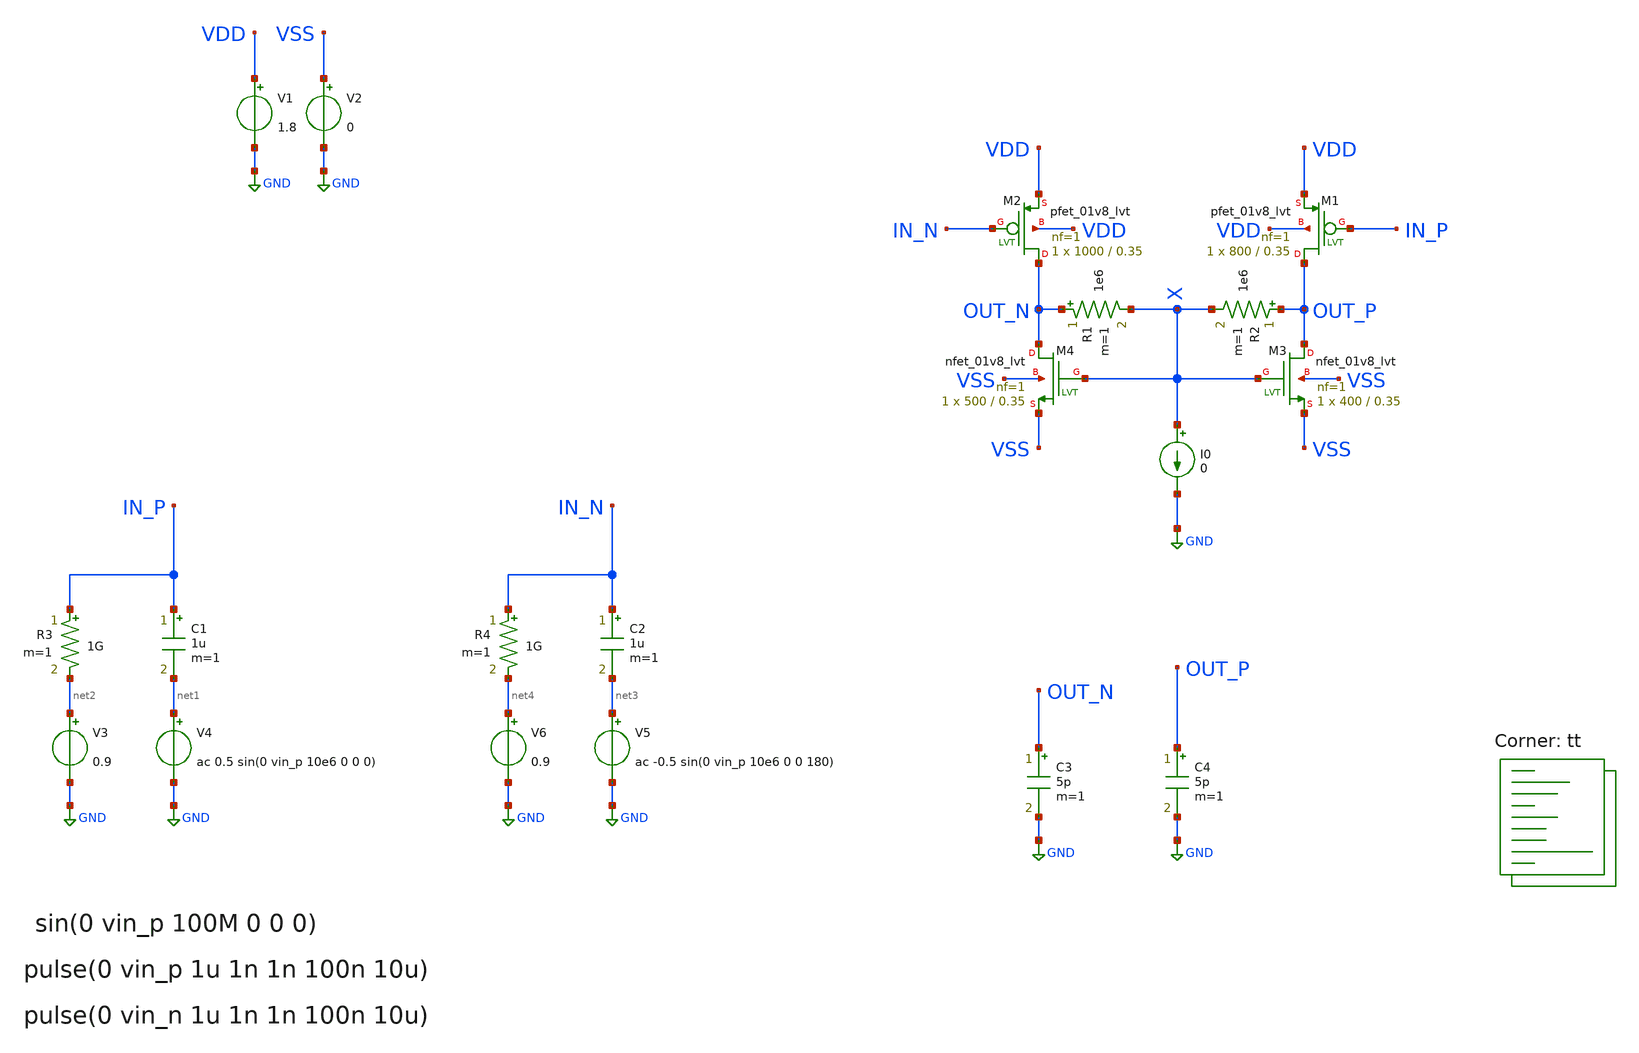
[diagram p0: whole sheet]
** sch_path: xschem/common_source.sch
**.subckt common_source
V1 VDD GND 1.8
.save i(v1)
V2 VSS GND 0
.save i(v2)
V4 net1 GND ac 0.5 sin(0 vin_p 10e6 0 0 0)
.save i(v4)
XM1 OUT_P IN_P VDD VDD sky130_fd_pr__pfet_01v8_lvt L=0.35 W=800 nf=1 ad='int((1 + 1)/2) * 800 / 1 * 0.29'
+ as='int((1 + 2)/2) * 800 / 1 * 0.29' pd='2*int((1 + 1)/2) * (800 / 1 + 0.29)' ps='2*int((1 + 2)/2) * (800 / 1 + 0.29)'
+ nrd='0.29 / 800 ' nrs='0.29 / 800 ' sa=0 sb=0 sd=0 mult=1 m=1
XM2 OUT_N IN_N VDD VDD sky130_fd_pr__pfet_01v8_lvt L=0.35 W=1000 nf=1 ad='int((1 + 1)/2) * 1000 / 1 * 0.29'
+ as='int((1 + 2)/2) * 1000 / 1 * 0.29' pd='2*int((1 + 1)/2) * (1000 / 1 + 0.29)' ps='2*int((1 + 2)/2) * (1000 / 1 + 0.29)'
+ nrd='0.29 / 1000 ' nrs='0.29 / 1000 ' sa=0 sb=0 sd=0 mult=1 m=1
XM3 OUT_P X VSS VSS sky130_fd_pr__nfet_01v8_lvt L=0.35 W=400 nf=1 ad='int((1 + 1)/2) * 400 / 1 * 0.29'
+ as='int((1 + 2)/2) * 400 / 1 * 0.29' pd='2*int((1 + 1)/2) * (400 / 1 + 0.29)' ps='2*int((1 + 2)/2) * (400 / 1 + 0.29)'
+ nrd='0.29 / 400 ' nrs='0.29 / 400 ' sa=0 sb=0 sd=0 mult=1 m=1
XM4 OUT_N X VSS VSS sky130_fd_pr__nfet_01v8_lvt L=0.35 W=500 nf=1 ad='int((1 + 1)/2) * 500 / 1 * 0.29'
+ as='int((1 + 2)/2) * 500 / 1 * 0.29' pd='2*int((1 + 1)/2) * (500 / 1 + 0.29)' ps='2*int((1 + 2)/2) * (500 / 1 + 0.29)'
+ nrd='0.29 / 500 ' nrs='0.29 / 500 ' sa=0 sb=0 sd=0 mult=1 m=1
I0 X GND 0
R1 OUT_N X 1e6 m=1
R2 OUT_P X 1e6 m=1
C1 IN_P net1 1u m=1
V3 net2 GND 0.9
.save i(v3)
R3 IN_P net2 1G m=1
V5 net3 GND ac -0.5 sin(0 vin_p 10e6 0 0 180)
.save i(v5)
C2 IN_N net3 1u m=1
V6 net4 GND 0.9
.save i(v6)
R4 IN_N net4 1G m=1
C3 OUT_N GND 5p m=1
C4 OUT_P GND 5p m=1
**** begin user architecture code


.temp 25

.param vin_p=1
.param vin_n= -1 * vin_p

.control
option savecurrents
option klu
option method=gear
option noacct
option noinit
save all


save @m.xm1.msky130_fd_pr__pfet_01v8_lvt[gm]
save @m.xm1.msky130_fd_pr__pfet_01v8_lvt[id]
save @m.xm1.msky130_fd_pr__pfet_01v8_lvt[vds]

save @m.xm2.msky130_fd_pr__pfet_01v8_lvt[gm]
save @m.xm2.msky130_fd_pr__pfet_01v8_lvt[id]
save @m.xm2.msky130_fd_pr__pfet_01v8_lvt[vds]

save @m.xm3.msky130_fd_pr__nfet_01v8_lvt[gm]
save @m.xm3.msky130_fd_pr__nfet_01v8_lvt[id]
save @m.xm3.msky130_fd_pr__nfet_01v8_lvt[vds]

save @m.xm4.msky130_fd_pr__nfet_01v8_lvt[gm]
save @m.xm4.msky130_fd_pr__nfet_01v8_lvt[id]
save @m.xm4.msky130_fd_pr__nfet_01v8_lvt[vds]




op
write common_source.raw

*vb1 sweep
*dc v3 0 1.8 0.1
*plot out_p
*plot @m.xm3.msky130_fd_pr__nfet_01v8_lvt[vds]

*vb2 sweep
*dc v4 0 1.8 0.1
*plot out_p
*plot @m.xm5.msky130_fd_pr__pfet_01v8_lvt[vds]

*vb3 sweep
*dc v5 0 1.8 0.1
*plot out_p
*plot @m.xm7.msky130_fd_pr__pfet_01v8_lvt[vds]

ac dec 10 1k 10G
let out_db = db(mag(out_p - out_n))
let out_ph = phase(out_p - out_n) / pi * 180
plot out_db
*plot out_ph
meas ac w_u WHEN out_db=0
meas ac p_x WHEN out_ph=0
meas ac phase_mar find out_ph AT=w_u
let w_u_mhz = w_u / 1e6
print w_u_mhz phase_mar

*dc i0 0 1u 1n
*plot out_p out_n

*tran 100p 2u
*plot in_p in_n
*plot out_p - out_n




.endc

.lib $::SKYWATER_MODELS/sky130.lib.spice tt
**** end user architecture code
**.ends
.GLOBAL GND
.end
